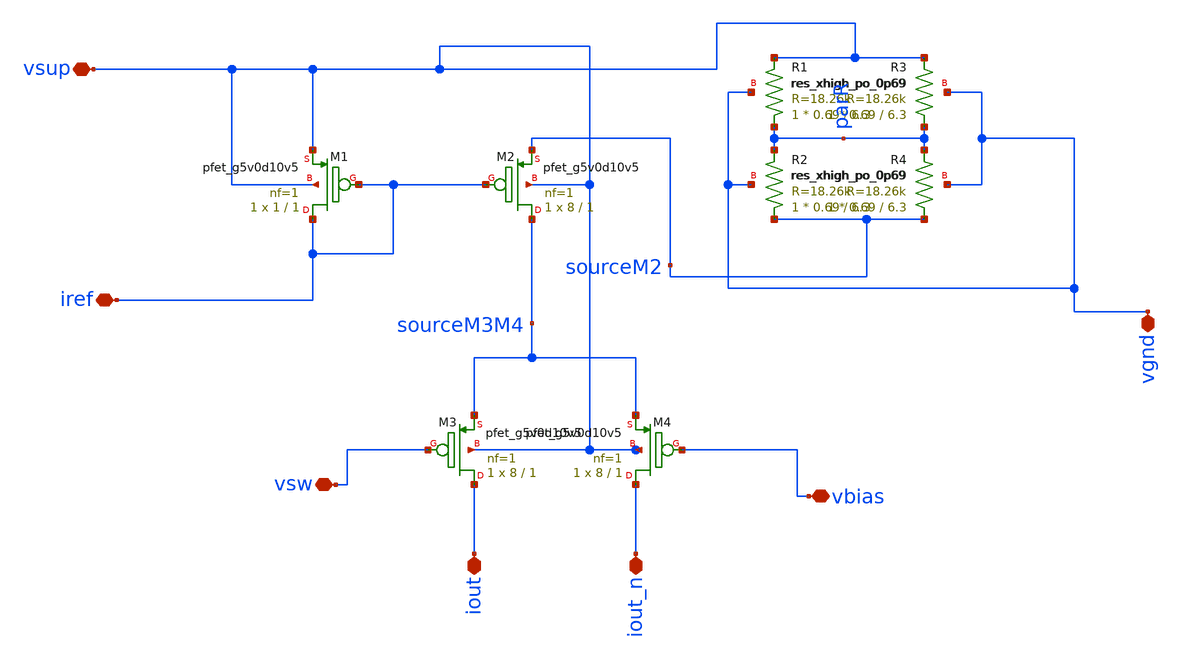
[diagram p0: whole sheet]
** sch_path: dev/dac_cell4/tb/dac_cell4.sch
**.subckt dac_cell4 vsup vgnd iref vsw iout iout_n vbias
*.iopin vsup
*.iopin vgnd
*.iopin iref
*.iopin vsw
*.iopin iout
*.iopin iout_n
*.iopin vbias
XM1 iref iref vsup vsup sky130_fd_pr__pfet_g5v0d10v5 L=1 W=1 nf=1 ad='int((nf+1)/2) * W/nf * 0.29' as='int((nf+2)/2) * W/nf * 0.29'
+ pd='2*int((nf+1)/2) * (W/nf + 0.29)' ps='2*int((nf+2)/2) * (W/nf + 0.29)' nrd='0.29 / W' nrs='0.29 / W'
+ sa=0 sb=0 sd=0 mult=1 m=1
XM2 sourceM3M4 iref sourceM2 vsup sky130_fd_pr__pfet_g5v0d10v5 L=1 W=8 nf=1 ad='int((nf+1)/2) * W/nf * 0.29'
+ as='int((nf+2)/2) * W/nf * 0.29' pd='2*int((nf+1)/2) * (W/nf + 0.29)' ps='2*int((nf+2)/2) * (W/nf + 0.29)'
+ nrd='0.29 / W' nrs='0.29 / W' sa=0 sb=0 sd=0 mult=1 m=1
XM3 iout vsw sourceM3M4 vsup sky130_fd_pr__pfet_g5v0d10v5 L=1 W=8 nf=1 ad='int((nf+1)/2) * W/nf * 0.29'
+ as='int((nf+2)/2) * W/nf * 0.29' pd='2*int((nf+1)/2) * (W/nf + 0.29)' ps='2*int((nf+2)/2) * (W/nf + 0.29)'
+ nrd='0.29 / W' nrs='0.29 / W' sa=0 sb=0 sd=0 mult=1 m=1
XM4 iout_n vbias sourceM3M4 vsup sky130_fd_pr__pfet_g5v0d10v5 L=1 W=8 nf=1 ad='int((nf+1)/2) * W/nf * 0.29'
+ as='int((nf+2)/2) * W/nf * 0.29' pd='2*int((nf+1)/2) * (W/nf + 0.29)' ps='2*int((nf+2)/2) * (W/nf + 0.29)'
+ nrd='0.29 / W' nrs='0.29 / W' sa=0 sb=0 sd=0 mult=1 m=1
XR1 parR vsup vgnd sky130_fd_pr__res_xhigh_po_0p69 L=6.3 mult=1 m=1
XR2 sourceM2 parR vgnd sky130_fd_pr__res_xhigh_po_0p69 L=6.3 mult=1 m=1
XR3 parR vsup vgnd sky130_fd_pr__res_xhigh_po_0p69 L=6.3 mult=1 m=1
XR4 sourceM2 parR vgnd sky130_fd_pr__res_xhigh_po_0p69 L=6.3 mult=1 m=1
**.ends
.end
